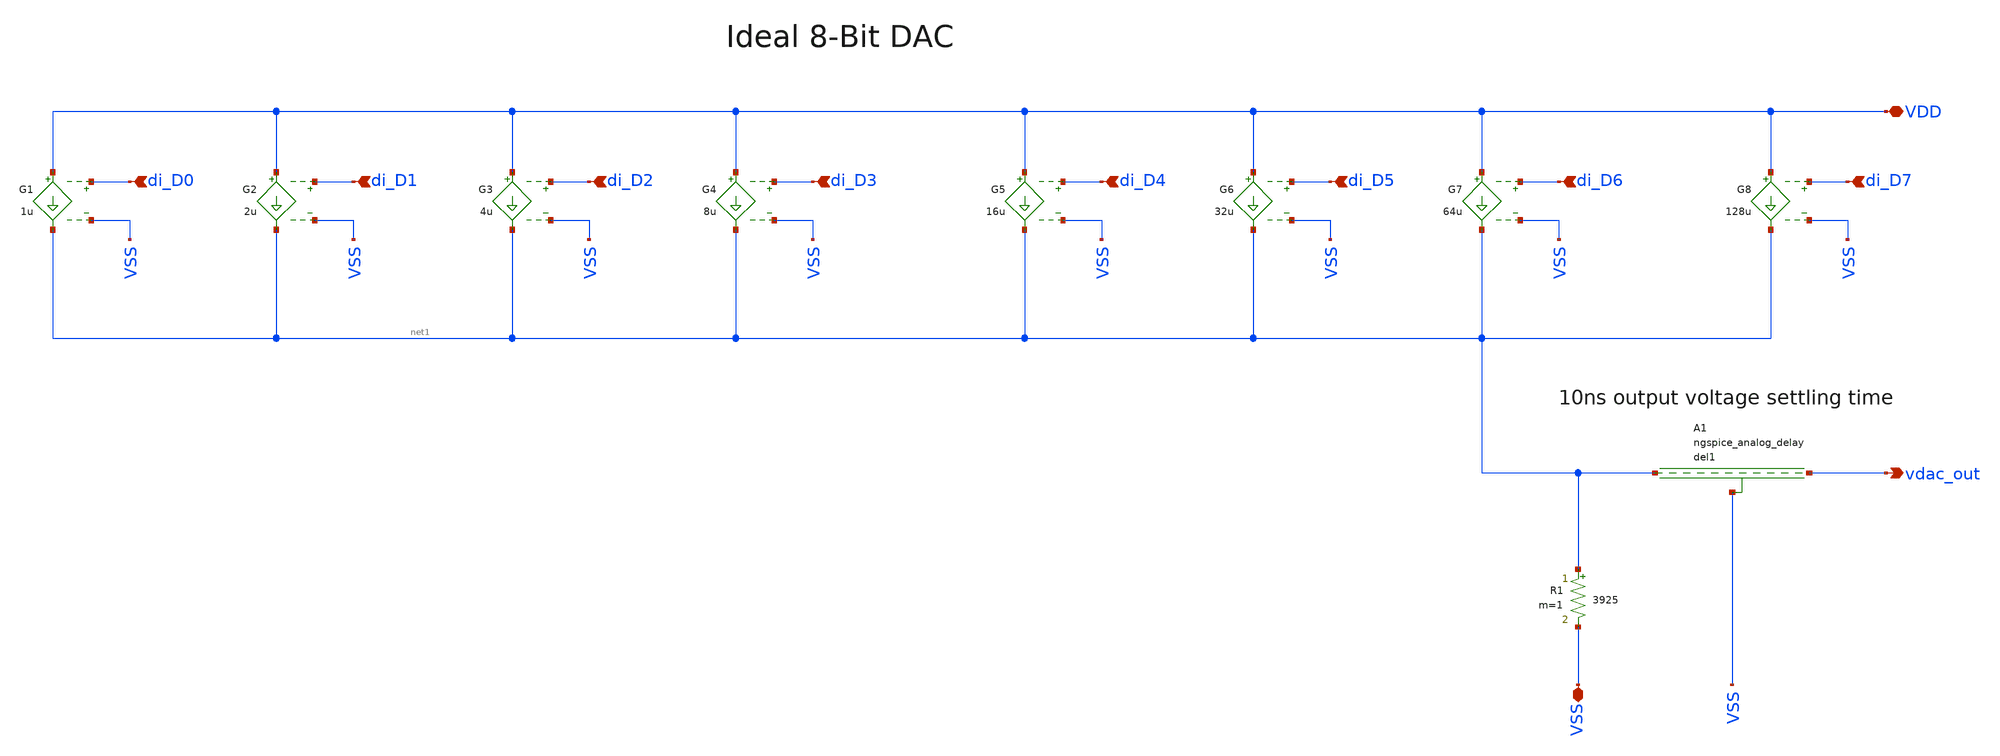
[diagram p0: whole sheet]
** sch_path: SG13G2_ATBS-ADC-main/xschem/dac/ideal/dac_ideal.sch
**.subckt dac_ideal vdac_out di_D0 VSS VDD di_D1 di_D2 di_D3 di_D4 di_D5 di_D6 di_D7
*.opin vdac_out
*.ipin di_D0
*.iopin VSS
*.iopin VDD
*.ipin di_D1
*.ipin di_D2
*.ipin di_D3
*.ipin di_D4
*.ipin di_D5
*.ipin di_D6
*.ipin di_D7
R1 net1 VSS 3925 m=1
G1 VDD net1 di_D0 VSS 1u
G2 VDD net1 di_D1 VSS 2u
G3 VDD net1 di_D2 VSS 4u
G4 VDD net1 di_D3 VSS 8u
G5 VDD net1 di_D4 VSS 16u
G6 VDD net1 di_D5 VSS 32u
G7 VDD net1 di_D6 VSS 64u
G8 VDD net1 di_D7 VSS 128u
A1 net1 vdac_out VSS del_subckt
.model del_subckt delay(delay=tsettle buffer_size=8192)
**.ends
.end
